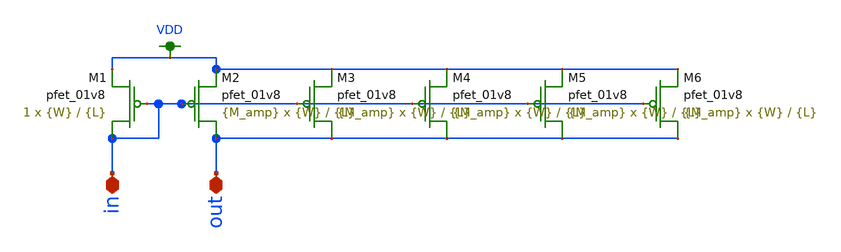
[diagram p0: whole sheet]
** sch_path: schemas/PMOS_gain_mirror.sch
**.subckt PMOS_gain_mirror in out
*.iopin in
*.iopin out
XM1 in in VDD VDD sky130_fd_pr__pfet_01v8 L={L} W={W} nf=1 ad='int((nf+1)/2) * W/nf * 0.29' as='int((nf+2)/2) * W/nf * 0.29'
+ pd='2*int((nf+1)/2) * (W/nf + 0.29)' ps='2*int((nf+2)/2) * (W/nf + 0.29)' nrd='0.29 / W' nrs='0.29 / W'
+ sa=0 sb=0 sd=0 mult=1 m=1
XM2 out in VDD VDD sky130_fd_pr__pfet_01v8 L={L} W={W} nf=1 ad='int((nf+1)/2) * W/nf * 0.29' as='int((nf+2)/2) * W/nf * 0.29'
+ pd='2*int((nf+1)/2) * (W/nf + 0.29)' ps='2*int((nf+2)/2) * (W/nf + 0.29)' nrd='0.29 / W' nrs='0.29 / W'
+ sa=0 sb=0 sd=0 mult={M_amp} m={M_amp}
XM3 out in VDD VDD sky130_fd_pr__pfet_01v8 L={L} W={W} nf=1 ad='int((nf+1)/2) * W/nf * 0.29' as='int((nf+2)/2) * W/nf * 0.29'
+ pd='2*int((nf+1)/2) * (W/nf + 0.29)' ps='2*int((nf+2)/2) * (W/nf + 0.29)' nrd='0.29 / W' nrs='0.29 / W'
+ sa=0 sb=0 sd=0 mult={M_amp} m={M_amp}
XM4 out in VDD VDD sky130_fd_pr__pfet_01v8 L={L} W={W} nf=1 ad='int((nf+1)/2) * W/nf * 0.29' as='int((nf+2)/2) * W/nf * 0.29'
+ pd='2*int((nf+1)/2) * (W/nf + 0.29)' ps='2*int((nf+2)/2) * (W/nf + 0.29)' nrd='0.29 / W' nrs='0.29 / W'
+ sa=0 sb=0 sd=0 mult={M_amp} m={M_amp}
XM5 out in VDD VDD sky130_fd_pr__pfet_01v8 L={L} W={W} nf=1 ad='int((nf+1)/2) * W/nf * 0.29' as='int((nf+2)/2) * W/nf * 0.29'
+ pd='2*int((nf+1)/2) * (W/nf + 0.29)' ps='2*int((nf+2)/2) * (W/nf + 0.29)' nrd='0.29 / W' nrs='0.29 / W'
+ sa=0 sb=0 sd=0 mult={M_amp} m={M_amp}
XM6 out in VDD VDD sky130_fd_pr__pfet_01v8 L={L} W={W} nf=1 ad='int((nf+1)/2) * W/nf * 0.29' as='int((nf+2)/2) * W/nf * 0.29'
+ pd='2*int((nf+1)/2) * (W/nf + 0.29)' ps='2*int((nf+2)/2) * (W/nf + 0.29)' nrd='0.29 / W' nrs='0.29 / W'
+ sa=0 sb=0 sd=0 mult={M_amp} m={M_amp}
**.ends
.GLOBAL VDD
.end
